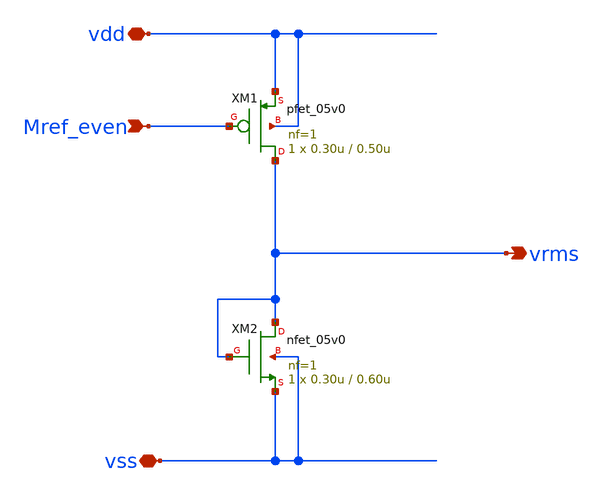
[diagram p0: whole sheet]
** sch_path: designs/libs/core_analog/rms_out/rms_out.sch
**.subckt rms_out Mref_even vdd vss vrms
*.ipin Mref_even
*.iopin vdd
*.iopin vss
*.opin vrms
XM1 vrms Mref_even vdd vdd pfet_05v0 L=0.50u W=0.30u nf=1 ad='int((nf+1)/2) * W/nf * 0.18u' as='int((nf+2)/2) * W/nf * 0.18u'
+ pd='2*int((nf+1)/2) * (W/nf + 0.18u)' ps='2*int((nf+2)/2) * (W/nf + 0.18u)' nrd='0.18u / W' nrs='0.18u / W'
+ sa=0 sb=0 sd=0 m=1
XM2 vrms vrms vss vss nfet_05v0 L=0.60u W=0.30u nf=1 ad='int((nf+1)/2) * W/nf * 0.18u' as='int((nf+2)/2) * W/nf * 0.18u'
+ pd='2*int((nf+1)/2) * (W/nf + 0.18u)' ps='2*int((nf+2)/2) * (W/nf + 0.18u)' nrd='0.18u / W' nrs='0.18u / W'
+ sa=0 sb=0 sd=0 m=1
**.ends
.end
